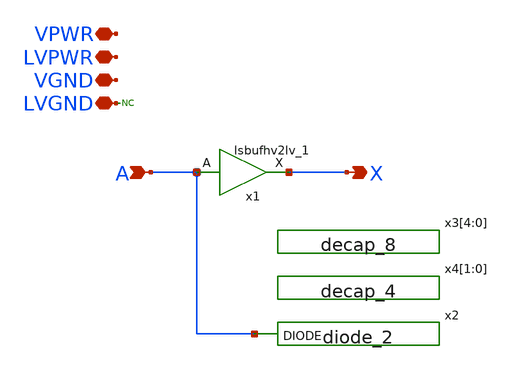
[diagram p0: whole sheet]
** sch_path: xschem/xres_buf.sch
**.subckt xres_buf A X VPWR LVPWR VGND LVGND
*.ipin A
*.opin X
*.iopin VPWR
*.iopin LVPWR
*.iopin VGND
*.iopin LVGND
x1 A LVPWR VGND VGND VPWR VPWR X sky130_fd_sc_hvl__lsbufhv2lv_1
x3[4] VGND VGND VPWR VPWR sky130_fd_sc_hvl__decap_8
x3[3] VGND VGND VPWR VPWR sky130_fd_sc_hvl__decap_8
x3[2] VGND VGND VPWR VPWR sky130_fd_sc_hvl__decap_8
x3[1] VGND VGND VPWR VPWR sky130_fd_sc_hvl__decap_8
x3[0] VGND VGND VPWR VPWR sky130_fd_sc_hvl__decap_8
x4[1] VGND VGND VPWR VPWR sky130_fd_sc_hvl__decap_4
x4[0] VGND VGND VPWR VPWR sky130_fd_sc_hvl__decap_4
* noconn LVGND
x2 A VGND VGND VPWR VPWR sky130_fd_sc_hvl__diode_2
**.ends
.end
